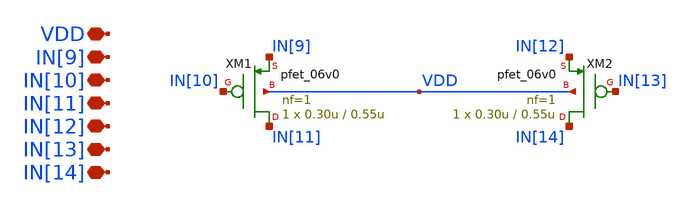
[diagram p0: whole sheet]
** sch_path: designs/libs/core_single-fet/pfet-vdd/pfet-vdd.sch
**.subckt pfet-vdd VDD IN[9] IN[10] IN[11] IN[12] IN[13] IN[14]
*.iopin VDD
*.iopin IN[9]
*.iopin IN[10]
*.iopin IN[11]
*.iopin IN[12]
*.iopin IN[13]
*.iopin IN[14]
XM1 IN[11] IN[10] IN[9] VDD pfet_06v0 L=0.55u W=0.30u nf=1 ad='int((nf+1)/2) * W/nf * 0.18u' as='int((nf+2)/2) * W/nf * 0.18u'
+ pd='2*int((nf+1)/2) * (W/nf + 0.18u)' ps='2*int((nf+2)/2) * (W/nf + 0.18u)' nrd='0.18u / W' nrs='0.18u / W'
+ sa=0 sb=0 sd=0 m=1
XM2 IN[14] IN[13] IN[12] VDD pfet_06v0 L=0.55u W=0.30u nf=1 ad='int((nf+1)/2) * W/nf * 0.18u' as='int((nf+2)/2) * W/nf * 0.18u'
+ pd='2*int((nf+1)/2) * (W/nf + 0.18u)' ps='2*int((nf+2)/2) * (W/nf + 0.18u)' nrd='0.18u / W' nrs='0.18u / W'
+ sa=0 sb=0 sd=0 m=1
**.ends
.end
